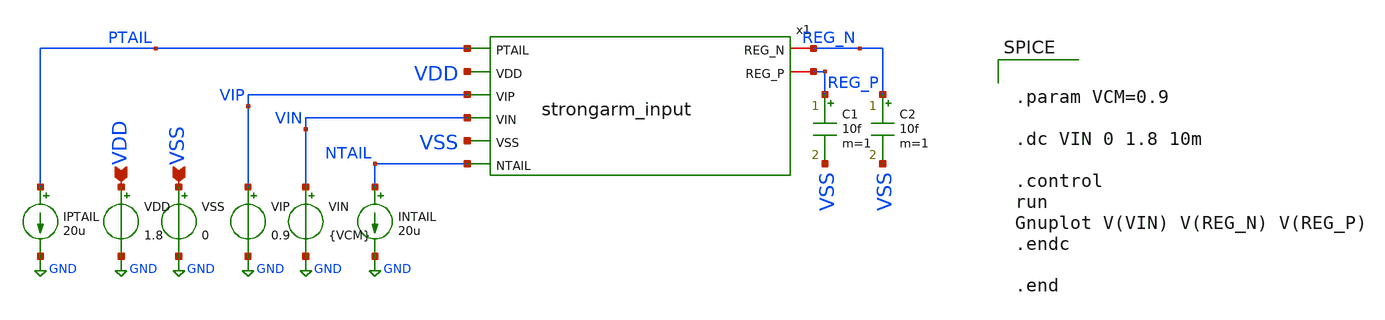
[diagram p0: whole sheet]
** sch_path: tb_strongarminput.sch
**.subckt tb_strongarminput VDD VSS
*.ipin VDD
*.ipin VSS
x1 PTAIL VDD REG_N REG_P VIP VIN VSS NTAIL strongarm_input
C1 REG_P VSS 10f m=1
C2 REG_N VSS 10f m=1
VDD VDD GND 1.8
VSS VSS GND 0
VIN VIN GND {VCM}
VIP VIP GND 0.9
INTAIL NTAIL GND 20u
IPTAIL PTAIL GND 20u
**** begin user architecture code


.param VCM=0.9

.dc VIN 0 1.8 10m

.control
run
Gnuplot V(VIN) V(REG_N) V(REG_P)
.endc

.end


** opencircuitdesign pdks install
.lib $::SKYWATER_MODELS/sky130.lib.spice tt

**** end user architecture code
**.ends

* expanding   symbol:  /home/master/Documents/6_bit_Flash_ADC/strongarm_input.sym # of pins=8
** sym_path: strongarm_input.sym
** sch_path: strongarm_input.sch
.subckt strongarm_input PTAIL VDD REG_N REG_P VIP VIN VSS NTAIL
*.ipin PTAIL
*.ipin NTAIL
*.iopin REG_P
*.iopin REG_N
*.ipin VSS
*.ipin VDD
*.ipin VIP
*.ipin VIN
XM1 REG_N VIN NTAIL VSS sky130_fd_pr__nfet_01v8 L=0.15 W=12 nf=2 ad='int((2 + 1)/2) * 12 / 2 * 0.29'
+ as='int((2 + 2)/2) * 12 / 2 * 0.29' pd='2*int((2 + 1)/2) * (12 / 2 + 0.29)' ps='2*int((2 + 2)/2) * (12 / 2 + 0.29)'
+ nrd='0.29 / 12 ' nrs='0.29 / 12 ' sa=0 sb=0 sd=0 mult=1 m=1
XM2 REG_P VIP NTAIL VSS sky130_fd_pr__nfet_01v8 L=0.15 W=12 nf=2 ad='int((2 + 1)/2) * 12 / 2 * 0.29'
+ as='int((2 + 2)/2) * 12 / 2 * 0.29' pd='2*int((2 + 1)/2) * (12 / 2 + 0.29)' ps='2*int((2 + 2)/2) * (12 / 2 + 0.29)'
+ nrd='0.29 / 12 ' nrs='0.29 / 12 ' sa=0 sb=0 sd=0 mult=1 m=1
XM3 REG_N VIN PTAIL VDD sky130_fd_pr__pfet_01v8 L=0.15 W=24 nf=2 ad='int((2 + 1)/2) * 24 / 2 * 0.29'
+ as='int((2 + 2)/2) * 24 / 2 * 0.29' pd='2*int((2 + 1)/2) * (24 / 2 + 0.29)' ps='2*int((2 + 2)/2) * (24 / 2 + 0.29)'
+ nrd='0.29 / 24 ' nrs='0.29 / 24 ' sa=0 sb=0 sd=0 mult=1 m=1
XM4 REG_P VIP PTAIL VDD sky130_fd_pr__pfet_01v8 L=0.15 W=24 nf=2 ad='int((2 + 1)/2) * 24 / 2 * 0.29'
+ as='int((2 + 2)/2) * 24 / 2 * 0.29' pd='2*int((2 + 1)/2) * (24 / 2 + 0.29)' ps='2*int((2 + 2)/2) * (24 / 2 + 0.29)'
+ nrd='0.29 / 24 ' nrs='0.29 / 24 ' sa=0 sb=0 sd=0 mult=1 m=1
.ends

.GLOBAL GND
.end
